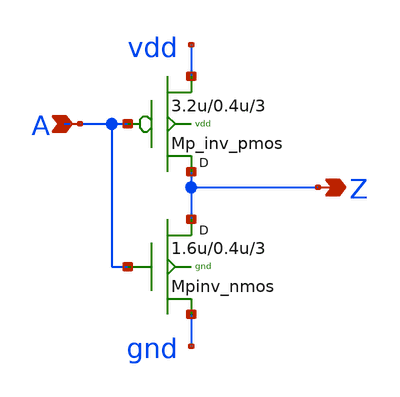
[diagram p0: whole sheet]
** sch_path: sram_2_64_scn4m_lcc/pinv_7.sch
**.subckt pinv_7 A Z
*.ipin A
*.opin Z
Mpinv_nmos Z A gnd gnd n w=1.6u l=0.4u m=3
Mp_inv_pmos Z A vdd vdd p w=3.2u l=0.4u m=3
**.ends
.end
